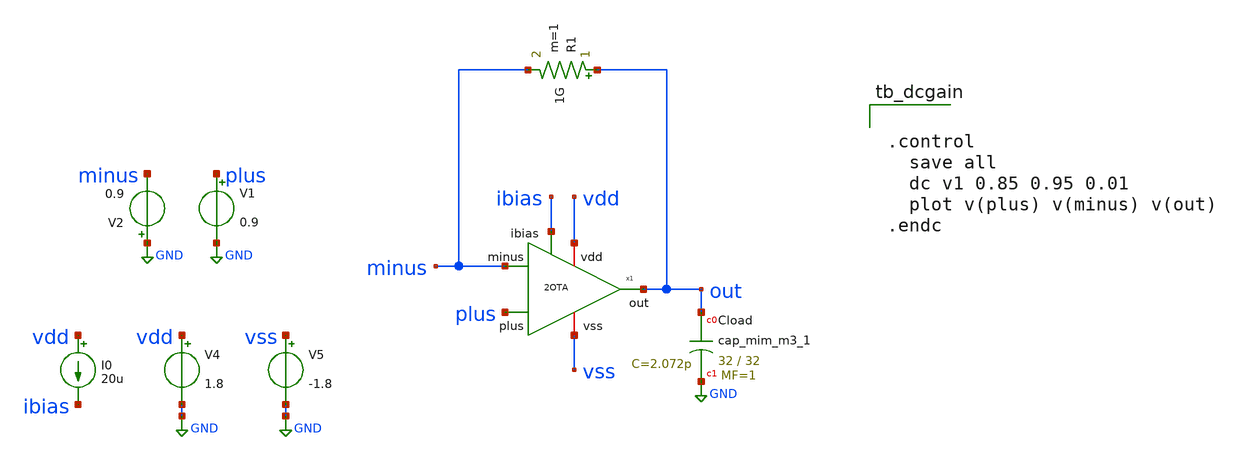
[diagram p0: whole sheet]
** sch_path: 2OTA_tb_compare.sch
**.subckt 2OTA_tb_compare
V1 plus GND 0.9
V2 GND minus 0.9
V4 vdd GND 1.8
V5 vss GND -1.8
I0 vdd ibias 20u
x1 vdd plus out minus ibias vss 2OTA
XCload out GND sky130_fd_pr__cap_mim_m3_1 W=32 L=32 MF=1 m=1
R1 out minus 1G m=1
**** begin user architecture code

** opencircuitdesign pdks install
.lib $::SKYWATER_MODELS/sky130.lib.spice tt



.control
  save all
  dc v1 0.85 0.95 0.01
  plot v(plus) v(minus) v(out)
.endc


**** end user architecture code
**.ends

* expanding   symbol:  2OTA.sym # of pins=6
** sym_path: 2OTA.sym
** sch_path: 2OTA.sch
.subckt 2OTA vdd plus out minus ibias vss
*.ipin ibias
*.ipin minus
*.ipin plus
*.iopin vdd
*.iopin vss
*.opin out
XM1 net2 net1 vdd vdd sky130_fd_pr__pfet_01v8 L=1 W=1.5 nf=1 ad='int((1 + 1)/2) * 1.5 / 1 * 0.29' as='int((1 + 2)/2) * 1.5 / 1 * 0.29'
+ pd='2*int((1 + 1)/2) * (1.5 / 1 + 0.29)' ps='2*int((1 + 2)/2) * (1.5 / 1 + 0.29)' nrd='0.29 / 1.5 ' nrs='0.29 / 1.5 '
+ sa=0 sb=0 sd=0 mult=1 m=1
XM2 net1 net1 vdd vdd sky130_fd_pr__pfet_01v8 L=1 W=1.5 nf=1 ad='int((1 + 1)/2) * 1.5 / 1 * 0.29' as='int((1 + 2)/2) * 1.5 / 1 * 0.29'
+ pd='2*int((1 + 1)/2) * (1.5 / 1 + 0.29)' ps='2*int((1 + 2)/2) * (1.5 / 1 + 0.29)' nrd='0.29 / 1.5 ' nrs='0.29 / 1.5 '
+ sa=0 sb=0 sd=0 mult=1 m=1
XM3 net1 minus net3 vss sky130_fd_pr__nfet_01v8 L=1 W=1.5 nf=1 ad='int((1 + 1)/2) * 1.5 / 1 * 0.29' as='int((1 + 2)/2) * 1.5 / 1 * 0.29'
+ pd='2*int((1 + 1)/2) * (1.5 / 1 + 0.29)' ps='2*int((1 + 2)/2) * (1.5 / 1 + 0.29)' nrd='0.29 / 1.5 ' nrs='0.29 / 1.5 '
+ sa=0 sb=0 sd=0 mult=1 m=1
XM4 net2 plus net3 vss sky130_fd_pr__nfet_01v8 L=1 W=1.5 nf=1 ad='int((1 + 1)/2) * 1.5 / 1 * 0.29' as='int((1 + 2)/2) * 1.5 / 1 * 0.29'
+ pd='2*int((1 + 1)/2) * (1.5 / 1 + 0.29)' ps='2*int((1 + 2)/2) * (1.5 / 1 + 0.29)' nrd='0.29 / 1.5 ' nrs='0.29 / 1.5 '
+ sa=0 sb=0 sd=0 mult=1 m=1
XM5 ibias ibias vss vss sky130_fd_pr__nfet_01v8 L=1 W=1.5 nf=1 ad='int((1 + 1)/2) * 1.5 / 1 * 0.29' as='int((1 + 2)/2) * 1.5 / 1 * 0.29'
+ pd='2*int((1 + 1)/2) * (1.5 / 1 + 0.29)' ps='2*int((1 + 2)/2) * (1.5 / 1 + 0.29)' nrd='0.29 / 1.5 ' nrs='0.29 / 1.5 '
+ sa=0 sb=0 sd=0 mult=1 m=1
XM6 net3 ibias vss vss sky130_fd_pr__nfet_01v8 L=1 W=1.5 nf=1 ad='int((1 + 1)/2) * 1.5 / 1 * 0.29' as='int((1 + 2)/2) * 1.5 / 1 * 0.29'
+ pd='2*int((1 + 1)/2) * (1.5 / 1 + 0.29)' ps='2*int((1 + 2)/2) * (1.5 / 1 + 0.29)' nrd='0.29 / 1.5 ' nrs='0.29 / 1.5 '
+ sa=0 sb=0 sd=0 mult=1 m=1
XM7 out net2 vdd vdd sky130_fd_pr__pfet_01v8 L=1 W=34 nf=4 ad='int((4 + 1)/2) * 34 / 4 * 0.29' as='int((4 + 2)/2) * 34 / 4 * 0.29'
+ pd='2*int((4 + 1)/2) * (34 / 4 + 0.29)' ps='2*int((4 + 2)/2) * (34 / 4 + 0.29)' nrd='0.29 / 34 ' nrs='0.29 / 34 '
+ sa=0 sb=0 sd=0 mult=1 m=1
XM8 out ibias vss vss sky130_fd_pr__nfet_01v8 L=1 W=13 nf=2 ad='int((2 + 1)/2) * 13 / 2 * 0.29' as='int((2 + 2)/2) * 13 / 2 * 0.29'
+ pd='2*int((2 + 1)/2) * (13 / 2 + 0.29)' ps='2*int((2 + 2)/2) * (13 / 2 + 0.29)' nrd='0.29 / 13 ' nrs='0.29 / 13 '
+ sa=0 sb=0 sd=0 mult=1 m=1
XC1 out net2 sky130_fd_pr__cap_mim_m3_1 W=15 L=15 MF=1 m=1
.ends

.GLOBAL GND
.end
